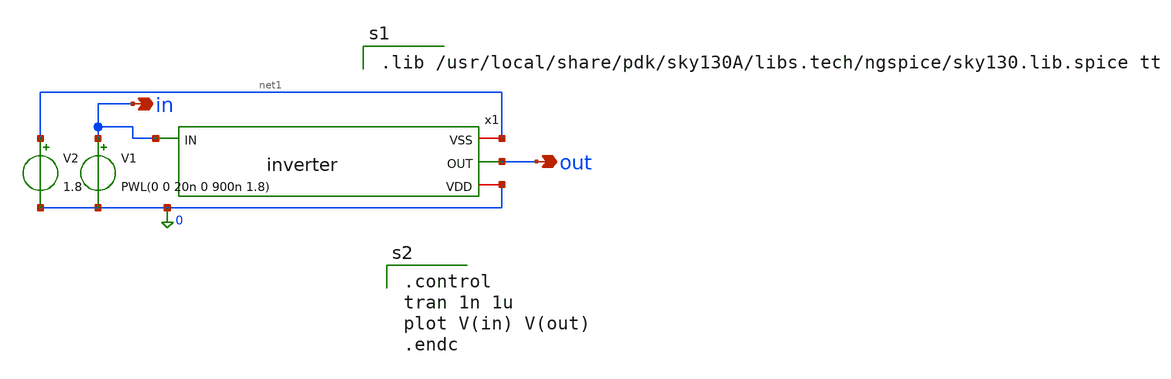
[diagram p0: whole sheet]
** sch_path: inverter/xschem/inverter_tb.sch
**.subckt inverter_tb out in
*.opin out
*.opin in
x1 net1 in out 0 inverter
V1 in 0 PWL(0 0 20n 0 900n 1.8)
V2 net1 0 1.8
**** begin user architecture code

.lib /usr/local/share/pdk/sky130A/libs.tech/ngspice/sky130.lib.spice tt


.control
tran 1n 1u
plot V(in) V(out)
.endc

**** end user architecture code
**.ends

* expanding   symbol:  inverter.sym # of pins=4
** sym_path: inverter.sym
** sch_path: inverter.sch
.subckt inverter VSS IN OUT VDD
*.ipin in
*.iopin vss
*.iopin vdd
*.opin out
XM1 out in vdd vdd sky130_fd_pr__pfet_01v8 L=0.18 W=3 nf=3 ad='int((3 + 1)/2) * 3 / 3 * 0.29' as='int((3 + 2)/2) * 3 / 3 * 0.29'
+ pd='2*int((3 + 1)/2) * (3 / 3 + 0.29)' ps='2*int((3 + 2)/2) * (3 / 3 + 0.29)' nrd='0.29 / 3 ' nrs='0.29 / 3 '
+ sa=0 sb=0 sd=0 mult=1 m=1
XM3 out in vss vss sky130_fd_pr__nfet_01v8 L=0.18 W=4.5 nf=3 ad='int((3 + 1)/2) * 4.5 / 3 * 0.29' as='int((3 + 2)/2) * 4.5 / 3 * 0.29'
+ pd='2*int((3 + 1)/2) * (4.5 / 3 + 0.29)' ps='2*int((3 + 2)/2) * (4.5 / 3 + 0.29)' nrd='0.29 / 4.5 ' nrs='0.29 / 4.5 '
+ sa=0 sb=0 sd=0 mult=1 m=1
.ends

.end
